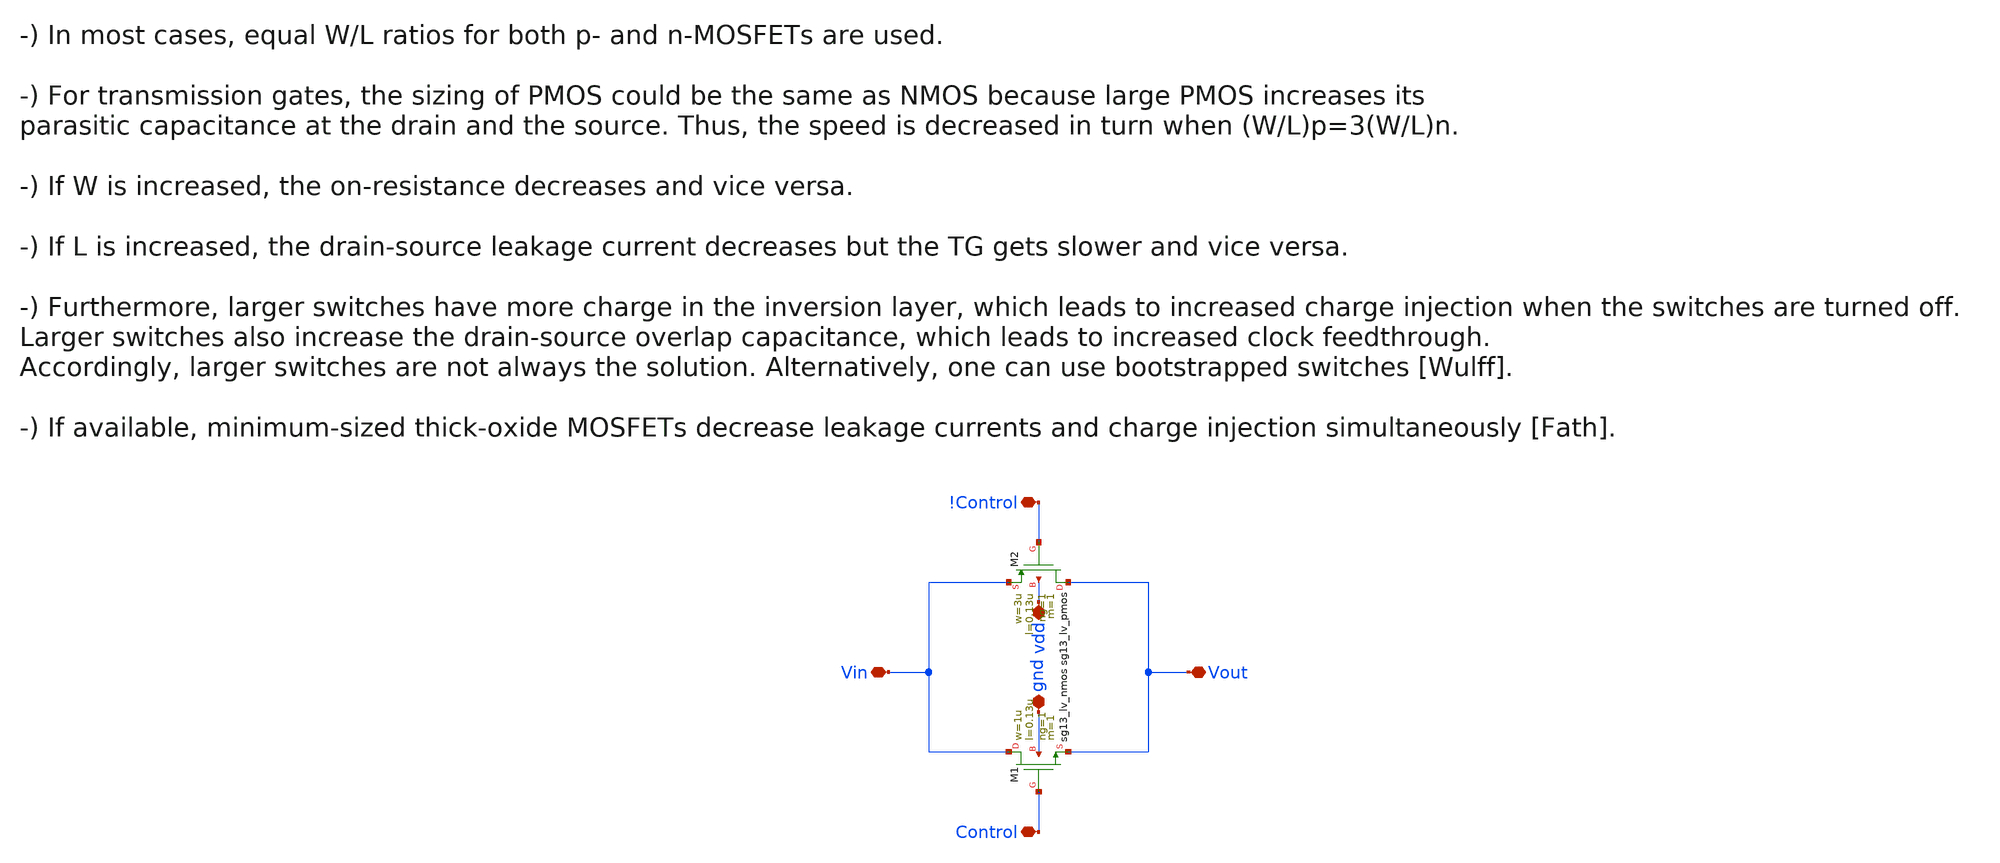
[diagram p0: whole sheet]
** sch_path: xschem/T_gate.sch
**.subckt T_gate Vout Vin !Control Control gnd vdd
*.iopin Vout
*.iopin Vin
*.iopin !Control
*.iopin Control
*.iopin gnd
*.iopin vdd
XM1 Vin Control Vout gnd sg13_lv_nmos w=1u l=0.13u ng=1 m=1 mm_ok=1
XM2 Vout !Control Vin vdd sg13_lv_pmos w=3u l=0.13u ng=1 m=1 mm_ok=1
**.ends
.end
